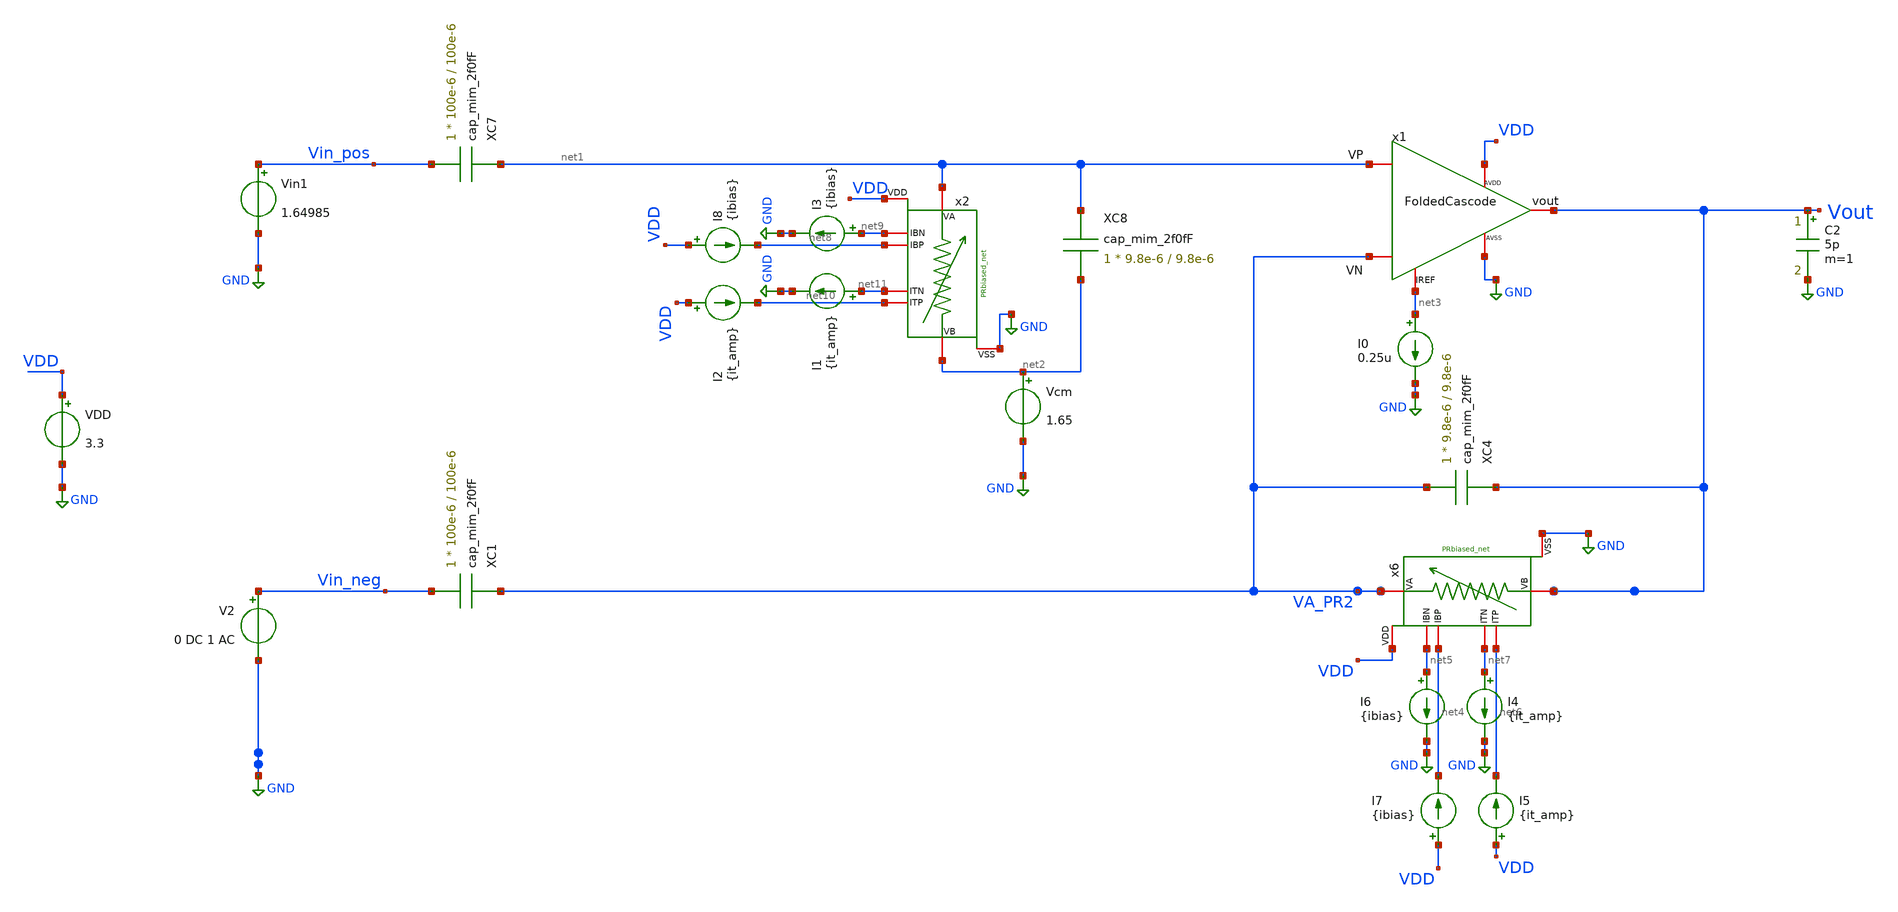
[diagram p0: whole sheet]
** sch_path: TIA_Filter/TB_filter_single_ac.sch
**.subckt TB_filter_single_ac
VDD VDD GND 3.3
C2 Vout GND 5p m=1
x1 net1 VA_PR2 Vout net3 VDD GND FoldedCascode
I0 net3 GND 0.25u
Vcm net2 GND 1.65
Vin1 Vin_pos GND 1.64985
V2 Vin_neg GND 0 DC 1 AC
x6 VA_PR2 Vout net5 net4 net7 net6 VDD GND PRbiased_net
I4 net7 GND {it_amp}
I5 VDD net6 {it_amp}
I6 net5 GND {ibias}
I7 VDD net4 {ibias}
x2 net1 net2 net9 net8 net11 net10 VDD GND PRbiased_net
I1 net11 GND {it_amp}
I2 VDD net10 {it_amp}
I3 net9 GND {ibias}
I8 VDD net8 {ibias}
XC7 net1 Vin_pos cap_mim_2f0fF c_width=100e-6 c_length=100e-6 m=1
XC8 net1 net2 cap_mim_2f0fF c_width=9.8e-6 c_length=9.8e-6 m=1
XC1 VA_PR2 Vin_neg cap_mim_2f0fF c_width=100e-6 c_length=100e-6 m=1
XC4 Vout VA_PR2 cap_mim_2f0fF c_width=9.8e-6 c_length=9.8e-6 m=1
**** begin user architecture code

.include $::180MCU_MODELS/design.ngspice
.lib $::180MCU_MODELS/sm141064.ngspice typical
.lib $::180MCU_MODELS/sm141064.ngspice cap_mim
.lib $::180MCU_MODELS/sm141064.ngspice res_typical
.lib $::180MCU_MODELS/sm141064.ngspice moscap_typical
.lib $::180MCU_MODELS/sm141064.ngspice mimcap_typical



.option gmin=1e-18
*.OPTION ABSTOL=1e-2

*.nodeset v(Vin_neg)=1.65
*.nodeset v(va_pr2)=1.65

*.nodeset all=1.65

.param ibias = 1p
.param it_amp = 2p

.control
save all

op
remzerovec
write TB_filter_single_ac.raw
set appendwrite

ac dec 10 1m 1e8
remzerovec
write TB_filter_single_ac.raw
set appendwrite


.endc


**** end user architecture code
**.ends
.GLOBAL GND
.end
